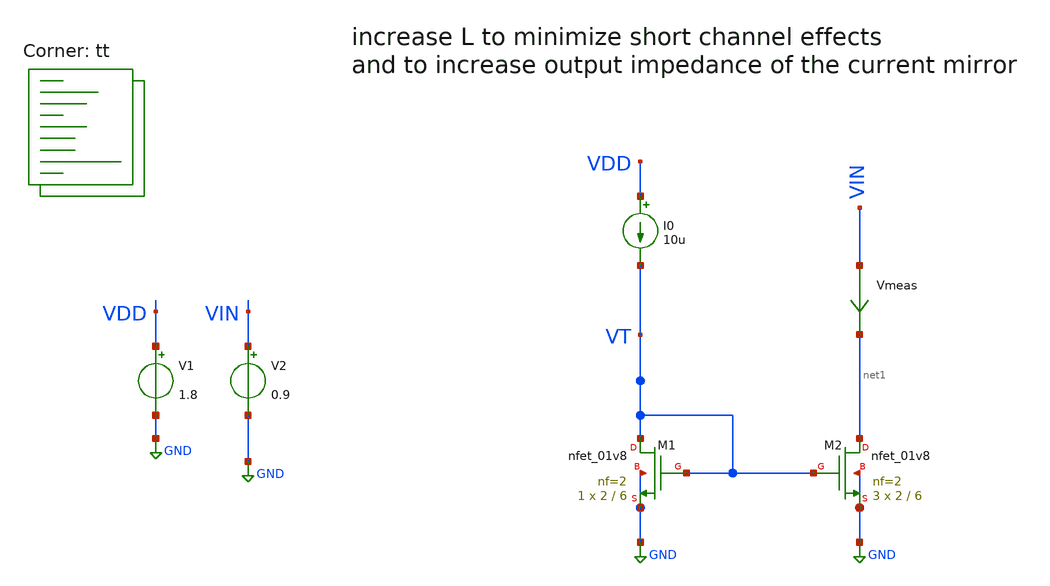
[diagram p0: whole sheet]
** sch_path: Analog_integrated_circuit_Design/chapter3/5/5.sch
**.subckt 5
V1 VDD GND 1.8
V2 VIN GND 0.9
Vmeas VIN net1 0
.save i(vmeas)
XM1 VT VT GND GND sky130_fd_pr__nfet_01v8 L=6 W=2 nf=2 ad='int((2 + 1)/2) * 2 / 2 * 0.29' as='int((2 + 2)/2) * 2 / 2 * 0.29'
+ pd='2*int((2 + 1)/2) * (2 / 2 + 0.29)' ps='2*int((2 + 2)/2) * (2 / 2 + 0.29)' nrd='0.29 / 2 ' nrs='0.29 / 2 '
+ sa=0 sb=0 sd=0 mult=1 m=1
I0 VDD VT 10u
XM2 net1 VT GND GND sky130_fd_pr__nfet_01v8 L=6 W=2 nf=2 ad='int((2 + 1)/2) * 2 / 2 * 0.29' as='int((2 + 2)/2) * 2 / 2 * 0.29'
+ pd='2*int((2 + 1)/2) * (2 / 2 + 0.29)' ps='2*int((2 + 2)/2) * (2 / 2 + 0.29)' nrd='0.29 / 2 ' nrs='0.29 / 2 '
+ sa=0 sb=0 sd=0 mult=3 m=3
**** begin user architecture code
.lib $::SKYWATER_MODELS/sky130.lib.spice tt

**************************************************************
**************************************************************
**************************************************************
**************************************************************
**************************************************************
*LIBs*********************************************************
**************************************************************
**************************************************************
**************************************************************
**************************************************************
**************************************************************
*.lib $::SKYWATER_MODELS/sky130.lib.spice tt
* chose the corners in the corner file
* tt_mm for mismatch
* ss ff sf fs standart corners
* ll hh lh hl capacitor and resistors corners
* mc for total process variation including corners
**************************************************************
**************************************************************
**************************************************************
**************************************************************
**************************************************************
*Corners/montecarlo options***********************************
**************************************************************
**************************************************************
**************************************************************
**************************************************************
**************************************************************
.TEMP 27
**************************************************************
**************************************************************
**************************************************************
**************************************************************
*SIMULATION and Plots*****************************************
**************************************************************
**************************************************************
**************************************************************
**************************************************************
.control
save all
dc V2 0 1.8 0.001
*dc simulation
plot i(Vmeas)
plot v(VT)
plot 1/deriv(i(Vmeas))
.endc

**** end user architecture code
**.ends
.GLOBAL GND
.end
